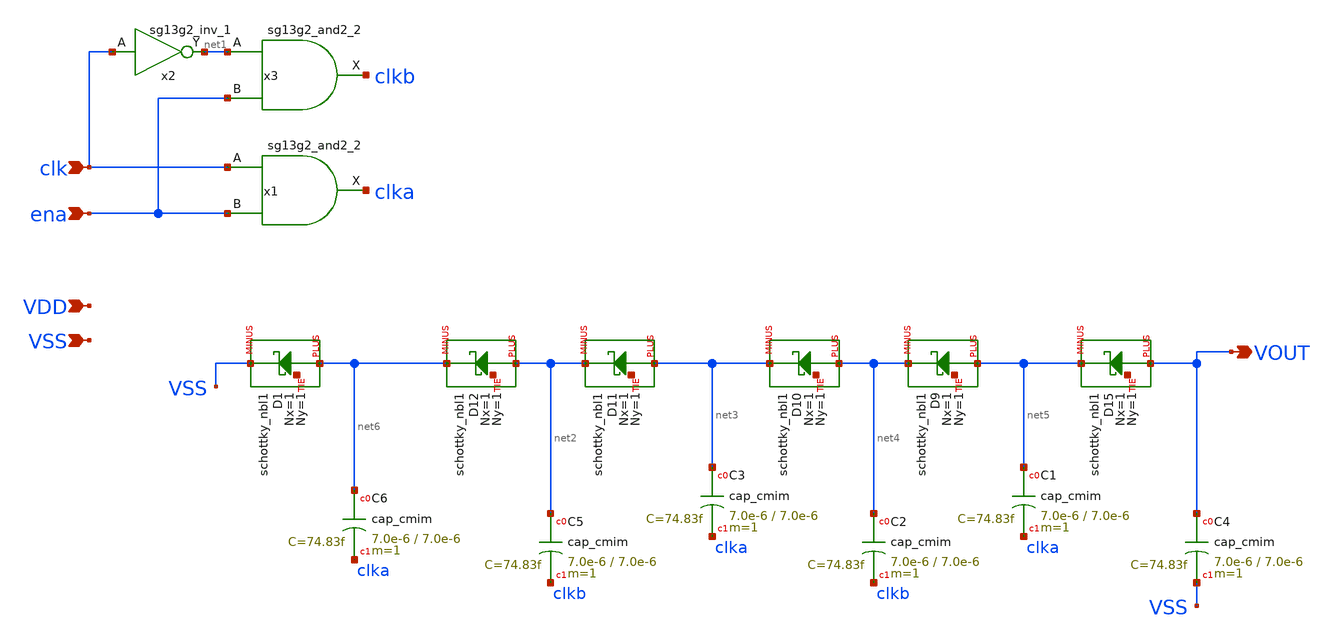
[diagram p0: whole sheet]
** sch_path: ihp130_cells/Schottky_NegChargePump/schottky_neg_pump.sch
**.subckt schottky_neg_pump clk ena VDD VSS VOUT
*.ipin clk
*.ipin ena
*.ipin VDD
*.ipin VSS
*.opin VOUT
XC4 VOUT VSS cap_cmim w=7.0e-6 l=7.0e-6 m=1 mm_ok=1
x1 clka clk ena VDD VSS sg13g2_and2_2
x2 net1 clk VDD VSS sg13g2_inv_1
x3 clkb net1 ena VDD VSS sg13g2_and2_2
XD15 VOUT net5 net7 schottky_nbl1 Nx=1 Ny=1
XD9 net5 net4 net8 schottky_nbl1 Nx=1 Ny=1
XD10 net4 net3 net9 schottky_nbl1 Nx=1 Ny=1
XD11 net3 net2 net10 schottky_nbl1 Nx=1 Ny=1
XD12 net2 net6 net11 schottky_nbl1 Nx=1 Ny=1
XC1 net5 clka cap_cmim w=7.0e-6 l=7.0e-6 m=1 mm_ok=1
XC2 net4 clkb cap_cmim w=7.0e-6 l=7.0e-6 m=1 mm_ok=1
XC3 net3 clka cap_cmim w=7.0e-6 l=7.0e-6 m=1 mm_ok=1
XC5 net2 clkb cap_cmim w=7.0e-6 l=7.0e-6 m=1 mm_ok=1
XD1 net6 VSS net12 schottky_nbl1 Nx=1 Ny=1
XC6 net6 clka cap_cmim w=7.0e-6 l=7.0e-6 m=1 mm_ok=1
**.ends

* expanding   symbol:  sg13g2_stdcells/sg13g2_and2_2.sym # of pins=3
** sym_path: sg13g2_stdcells/sg13g2_and2_2.sym
** sch_path: sg13g2_stdcells/sg13g2_and2_2.sch
.subckt sg13g2_and2_2 X A B VDD VSS
*.ipin A
*.ipin B
*.opin X
*.iopin VDD
*.iopin VSS
XM1 net1 A net2 VSS sg13_lv_nmos w=640.00n l=130.00n ng=1 m=1 mm_ok=1
XM2 net2 B VSS VSS sg13_lv_nmos w=640.00n l=130.00n ng=1 m=1 mm_ok=1
XM3 X net1 VSS VSS sg13_lv_nmos w=1.48u l=130.00n ng=2 m=1 mm_ok=1
XM4 net1 B VDD VDD sg13_lv_pmos w=840.00n l=130.00n ng=1 m=1 mm_ok=1
XM5 net1 A VDD VDD sg13_lv_pmos w=840.00n l=130.00n ng=1 m=1 mm_ok=1
XM6 X net1 VDD VDD sg13_lv_pmos w=2.24u l=130.00n ng=2 m=1 mm_ok=1
.ends


* expanding   symbol:  sg13g2_stdcells/sg13g2_inv_1.sym # of pins=2
** sym_path: sg13g2_stdcells/sg13g2_inv_1.sym
** sch_path: sg13g2_stdcells/sg13g2_inv_1.sch
.subckt sg13g2_inv_1 Y A VDD VSS
*.opin Y
*.ipin A
*.iopin VDD
*.iopin VSS
XM1 Y A VSS VSS sg13_lv_nmos w=740.00n l=130.00n ng=1 m=1 mm_ok=1
XM2 Y A VDD VDD sg13_lv_pmos w=1.12u l=130.00n ng=1 m=1 mm_ok=1
.ends

.end
